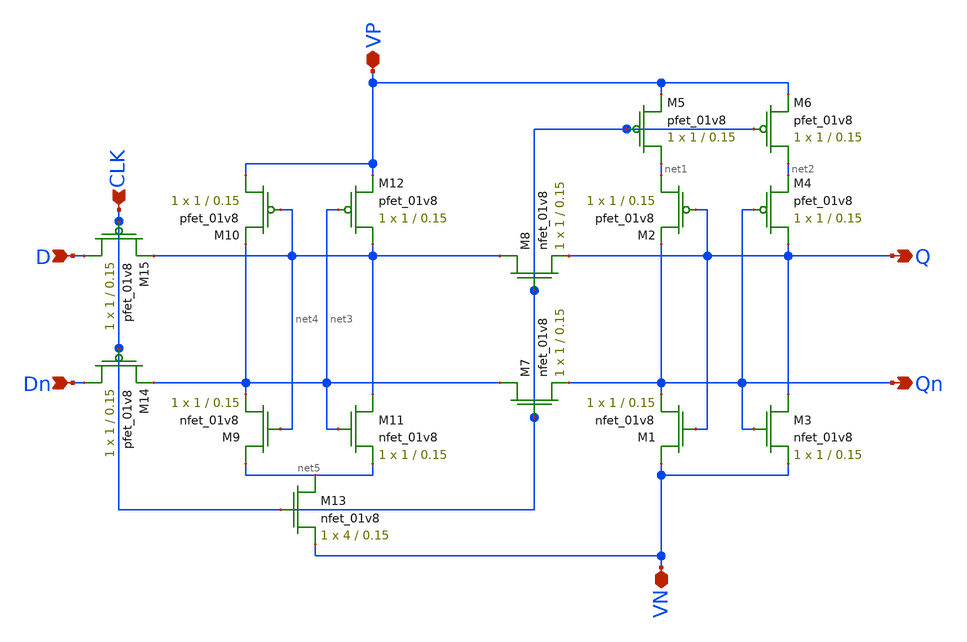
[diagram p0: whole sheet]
** sch_path: csrl_flipflop.sch
**.subckt csrl_flipflop D Dn CLK VP VN Q Qn
*.ipin D
*.ipin Dn
*.ipin CLK
*.iopin VP
*.iopin VN
*.opin Q
*.opin Qn
XM1 VN Q Qn GND sky130_fd_pr__nfet_01v8 L=0.15 W=1 nf=1 ad='int((nf+1)/2) * W/nf * 0.29' as='int((nf+2)/2) * W/nf * 0.29'
+ pd='2*int((nf+1)/2) * (W/nf + 0.29)' ps='2*int((nf+2)/2) * (W/nf + 0.29)' nrd='0.29 / W' nrs='0.29 / W'
+ sa=0 sb=0 sd=0 mult=1 m=1
XM2 net1 Q Qn VDD sky130_fd_pr__pfet_01v8 L=0.15 W=1 nf=1 ad='int((nf+1)/2) * W/nf * 0.29' as='int((nf+2)/2) * W/nf * 0.29'
+ pd='2*int((nf+1)/2) * (W/nf + 0.29)' ps='2*int((nf+2)/2) * (W/nf + 0.29)' nrd='0.29 / W' nrs='0.29 / W'
+ sa=0 sb=0 sd=0 mult=1 m=1
XM3 Q Qn VN GND sky130_fd_pr__nfet_01v8 L=0.15 W=1 nf=1 ad='int((nf+1)/2) * W/nf * 0.29' as='int((nf+2)/2) * W/nf * 0.29'
+ pd='2*int((nf+1)/2) * (W/nf + 0.29)' ps='2*int((nf+2)/2) * (W/nf + 0.29)' nrd='0.29 / W' nrs='0.29 / W'
+ sa=0 sb=0 sd=0 mult=1 m=1
XM4 Q Qn net2 VDD sky130_fd_pr__pfet_01v8 L=0.15 W=1 nf=1 ad='int((nf+1)/2) * W/nf * 0.29' as='int((nf+2)/2) * W/nf * 0.29'
+ pd='2*int((nf+1)/2) * (W/nf + 0.29)' ps='2*int((nf+2)/2) * (W/nf + 0.29)' nrd='0.29 / W' nrs='0.29 / W'
+ sa=0 sb=0 sd=0 mult=1 m=1
XM5 net1 CLK VP VDD sky130_fd_pr__pfet_01v8 L=0.15 W=1 nf=1 ad='int((nf+1)/2) * W/nf * 0.29' as='int((nf+2)/2) * W/nf * 0.29'
+ pd='2*int((nf+1)/2) * (W/nf + 0.29)' ps='2*int((nf+2)/2) * (W/nf + 0.29)' nrd='0.29 / W' nrs='0.29 / W'
+ sa=0 sb=0 sd=0 mult=1 m=1
XM6 net2 CLK VP VDD sky130_fd_pr__pfet_01v8 L=0.15 W=1 nf=1 ad='int((nf+1)/2) * W/nf * 0.29' as='int((nf+2)/2) * W/nf * 0.29'
+ pd='2*int((nf+1)/2) * (W/nf + 0.29)' ps='2*int((nf+2)/2) * (W/nf + 0.29)' nrd='0.29 / W' nrs='0.29 / W'
+ sa=0 sb=0 sd=0 mult=1 m=1
XM7 net3 CLK Qn GND sky130_fd_pr__nfet_01v8 L=0.15 W=1 nf=1 ad='int((nf+1)/2) * W/nf * 0.29' as='int((nf+2)/2) * W/nf * 0.29'
+ pd='2*int((nf+1)/2) * (W/nf + 0.29)' ps='2*int((nf+2)/2) * (W/nf + 0.29)' nrd='0.29 / W' nrs='0.29 / W'
+ sa=0 sb=0 sd=0 mult=1 m=1
XM8 net4 CLK Q GND sky130_fd_pr__nfet_01v8 L=0.15 W=1 nf=1 ad='int((nf+1)/2) * W/nf * 0.29' as='int((nf+2)/2) * W/nf * 0.29'
+ pd='2*int((nf+1)/2) * (W/nf + 0.29)' ps='2*int((nf+2)/2) * (W/nf + 0.29)' nrd='0.29 / W' nrs='0.29 / W'
+ sa=0 sb=0 sd=0 mult=1 m=1
XM9 net5 net4 net3 GND sky130_fd_pr__nfet_01v8 L=0.15 W=1 nf=1 ad='int((nf+1)/2) * W/nf * 0.29' as='int((nf+2)/2) * W/nf * 0.29'
+ pd='2*int((nf+1)/2) * (W/nf + 0.29)' ps='2*int((nf+2)/2) * (W/nf + 0.29)' nrd='0.29 / W' nrs='0.29 / W'
+ sa=0 sb=0 sd=0 mult=1 m=1
XM10 VP net4 net3 VDD sky130_fd_pr__pfet_01v8 L=0.15 W=1 nf=1 ad='int((nf+1)/2) * W/nf * 0.29' as='int((nf+2)/2) * W/nf * 0.29'
+ pd='2*int((nf+1)/2) * (W/nf + 0.29)' ps='2*int((nf+2)/2) * (W/nf + 0.29)' nrd='0.29 / W' nrs='0.29 / W'
+ sa=0 sb=0 sd=0 mult=1 m=1
XM11 net4 net3 net5 GND sky130_fd_pr__nfet_01v8 L=0.15 W=1 nf=1 ad='int((nf+1)/2) * W/nf * 0.29' as='int((nf+2)/2) * W/nf * 0.29'
+ pd='2*int((nf+1)/2) * (W/nf + 0.29)' ps='2*int((nf+2)/2) * (W/nf + 0.29)' nrd='0.29 / W' nrs='0.29 / W'
+ sa=0 sb=0 sd=0 mult=1 m=1
XM12 net4 net3 VP VDD sky130_fd_pr__pfet_01v8 L=0.15 W=1 nf=1 ad='int((nf+1)/2) * W/nf * 0.29' as='int((nf+2)/2) * W/nf * 0.29'
+ pd='2*int((nf+1)/2) * (W/nf + 0.29)' ps='2*int((nf+2)/2) * (W/nf + 0.29)' nrd='0.29 / W' nrs='0.29 / W'
+ sa=0 sb=0 sd=0 mult=1 m=1
XM13 net5 CLK VN GND sky130_fd_pr__nfet_01v8 L=0.15 W=4 nf=1 ad='int((nf+1)/2) * W/nf * 0.29' as='int((nf+2)/2) * W/nf * 0.29'
+ pd='2*int((nf+1)/2) * (W/nf + 0.29)' ps='2*int((nf+2)/2) * (W/nf + 0.29)' nrd='0.29 / W' nrs='0.29 / W'
+ sa=0 sb=0 sd=0 mult=1 m=1
XM14 Dn CLK net3 VDD sky130_fd_pr__pfet_01v8 L=0.15 W=1 nf=1 ad='int((nf+1)/2) * W/nf * 0.29' as='int((nf+2)/2) * W/nf * 0.29'
+ pd='2*int((nf+1)/2) * (W/nf + 0.29)' ps='2*int((nf+2)/2) * (W/nf + 0.29)' nrd='0.29 / W' nrs='0.29 / W'
+ sa=0 sb=0 sd=0 mult=1 m=1
XM15 D CLK net4 VDD sky130_fd_pr__pfet_01v8 L=0.15 W=1 nf=1 ad='int((nf+1)/2) * W/nf * 0.29' as='int((nf+2)/2) * W/nf * 0.29'
+ pd='2*int((nf+1)/2) * (W/nf + 0.29)' ps='2*int((nf+2)/2) * (W/nf + 0.29)' nrd='0.29 / W' nrs='0.29 / W'
+ sa=0 sb=0 sd=0 mult=1 m=1
**.ends
.end
